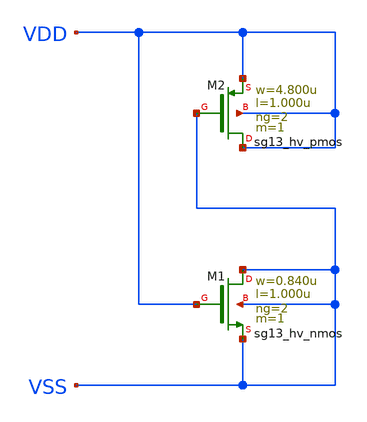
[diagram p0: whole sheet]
** sch_path: ihp-sg13g2/libs.ref/sg13g2_stdcell_hv/sch/xschem/sg13g2_hv_decap_8.sch
* Copyright 2023 IHP PDK Authors
* Licensed under the Apache License, Version 2.0 (the "License");
* you may not use this file except in compliance with the License.
* You may obtain a copy of the License at
* https://www.apache.org/licenses/LICENSE-2.0
* Unless required by applicable law or agreed to in writing, software
* distributed under the License is distributed on an "AS IS" BASIS,
* WITHOUT WARRANTIES OR CONDITIONS OF ANY KIND, either express or implied.
* See the License for the specific language governing permissions and
* limitations under the License.
**.subckt sg13g2_hv_decap_8
XM1 VSS VDD VSS VSS sg13_hv_nmos w=0.840u l=1.000u ng=2 m=1 mm_ok=1
XM2 VDD VSS VDD VDD sg13_hv_pmos w=4.800u l=1.000u ng=2 m=1 mm_ok=1
**.ends
.end
